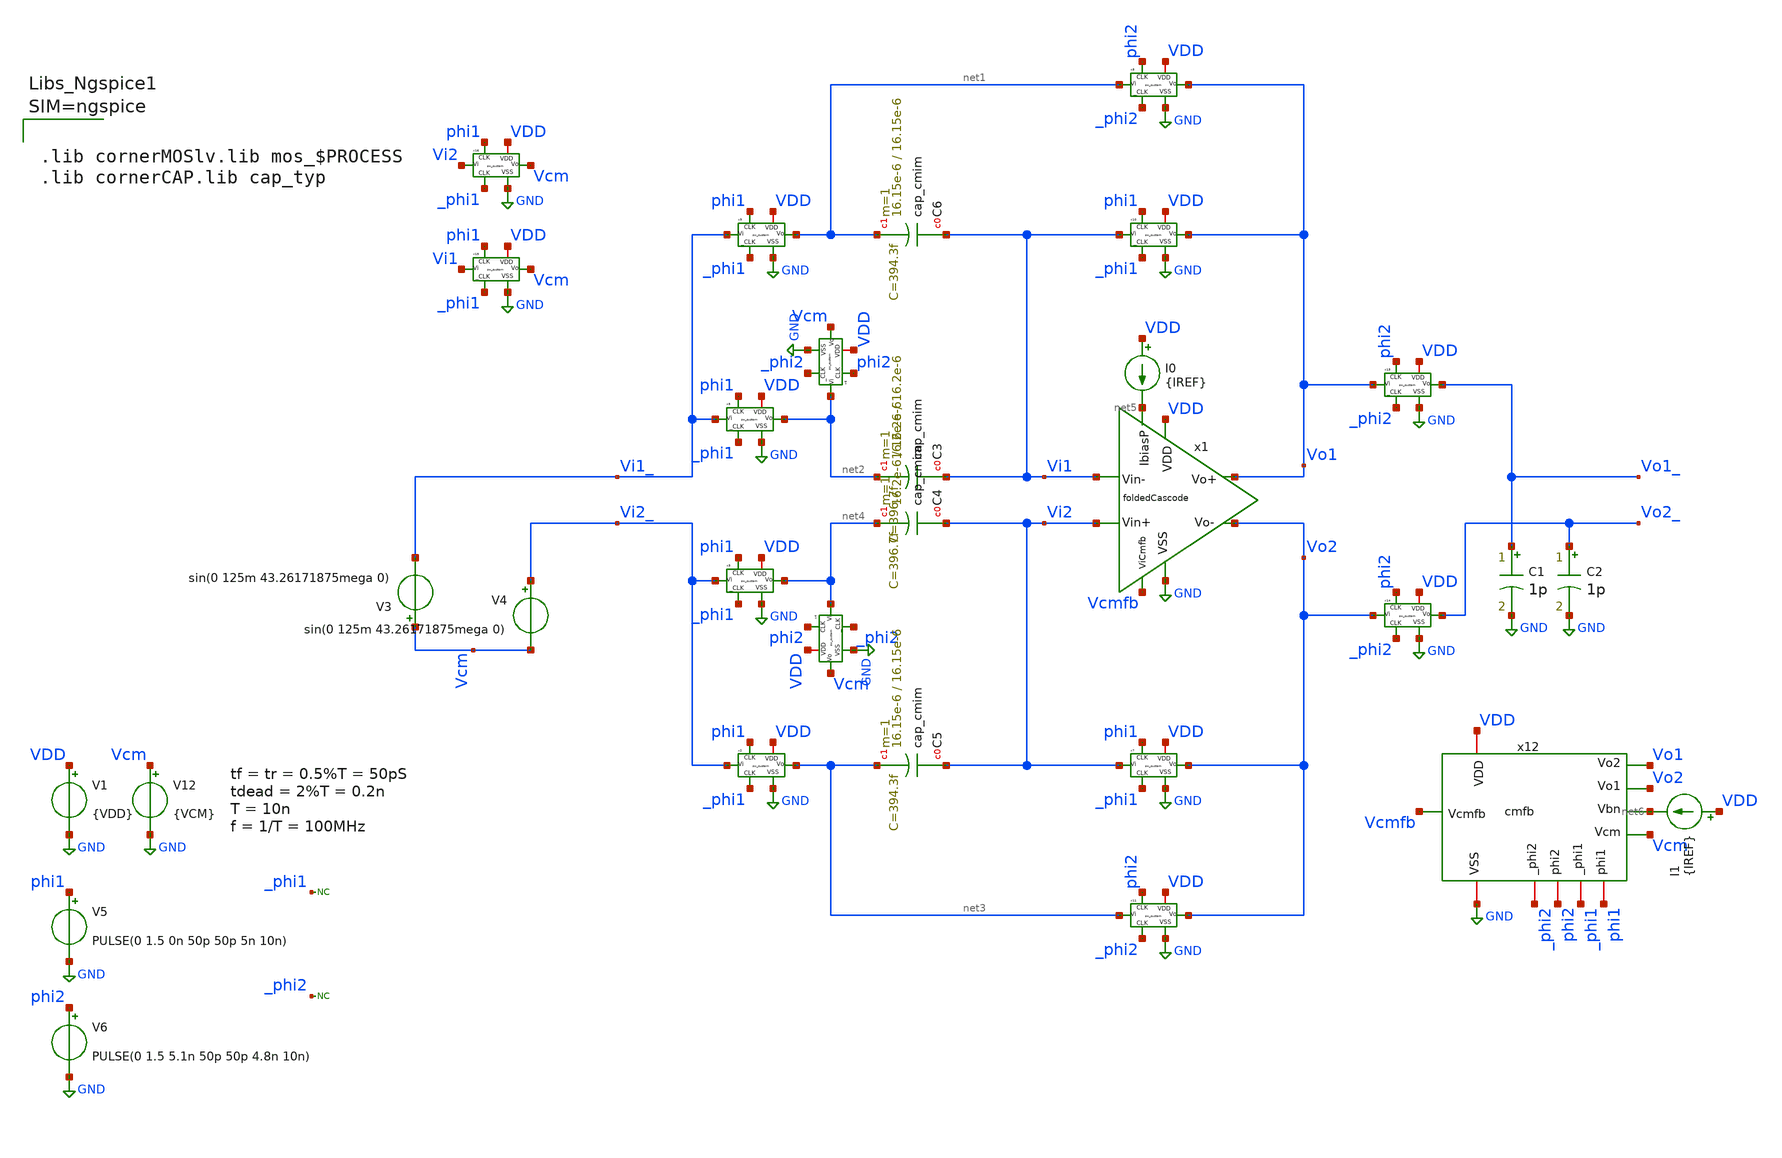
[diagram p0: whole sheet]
** sch_path: sch/AutoTestbench/tb/HFcloseLoop.sch
**.subckt HFcloseLoop
x1 VDD GND Vcmfb net5 Vo1 Vo2 Vi1 Vi2 foldedCascode
V1 VDD GND {VDD}
I0 VDD net5 {IREF}
V5 phi1 GND PULSE(0 1.5 0n 50p 50p 5n 10n)
V6 phi2 GND PULSE(0 1.5 5.1n 50p 50p 4.8n 10n)
x2 phi1 GND net3 Vi2_ VDD _phi1 sw_custom
x3 phi1 GND net4 Vi2_ VDD _phi1 sw_custom
x6 phi2 GND Vcm net2 VDD _phi2 sw_custom
x7 phi1 GND Vo2 Vi2 VDD _phi1 sw_custom
x8 phi2 GND Vo1 net1 VDD _phi2 sw_custom
x10 phi1 GND Vo1 Vi1 VDD _phi1 sw_custom
x9 phi1 GND net1 Vi1_ VDD _phi1 sw_custom
x11 phi2 GND Vo2 net3 VDD _phi2 sw_custom
x12 VDD GND phi1 _phi1 phi2 _phi2 Vcm net6 Vcmfb Vo2 Vo1 cmfb
x5 phi1 GND net2 Vi1_ VDD _phi1 sw_custom
x13 phi2 GND Vo1_ Vo1 VDD _phi2 sw_custom
x14 phi2 GND Vo2_ Vo2 VDD _phi2 sw_custom
V12 Vcm GND {VCM}
x15 phi1 GND Vcm Vi1 VDD _phi1 sw_custom
x16 phi1 GND Vcm Vi2 VDD _phi1 sw_custom
V3 Vcm Vi1_ sin(0 125m 43.26171875mega 0)
V4 Vi2_ Vcm sin(0 125m 43.26171875mega 0)
C1 Vo1_ GND 1p m=1
C2 Vo2_ GND 1p m=1
x4 phi2 GND Vcm net4 VDD _phi2 sw_custom
* noconn _phi1
* noconn _phi2
I1 VDD net6 {IREF}
XC3 Vi1 net2 cap_cmim w=16.2e-6 l=16.2e-6 m=1 mm_ok=1
XC5 Vi2 net3 cap_cmim w=16.15e-6 l=16.15e-6 m=1 mm_ok=1
XC6 Vi1 net1 cap_cmim w=16.15e-6 l=16.15e-6 m=1 mm_ok=1
XC4 Vi2 net4 cap_cmim w=16.2e-6 l=16.2e-6 m=1 mm_ok=1
**** begin user architecture code



.lib cornerMOSlv.lib mos_$PROCESS
.lib cornerCAP.lib cap_typ





.temp $TEMP
.model SW1 SW(Ron=200 Roff=10G Vt=0.4 Vh=0.1)
.nodeset v(Vo1)=0.6 v(Vo2)=0.6 v(Vi1)=0.6 v(Vi2)=0.6
.param VDD=$VDD
.param IREF=$IREF
.param VCM=$VCM
.control
op
tran 100p 12u
let vcm = (v(Vo1) + v(Vo2)) / 2
meas tran vcm_avg AVG vcm FROM=1u TO=3u
let Vinn = v(Vi1_)-v(Vi2_)
let Voutt = v(Vo1_)-v(Vo2_)
meas tran vin_pp  PP Vinn from=1u to=3u
meas tran vout_pp PP Voutt from=1u to=3u

let gain = vout_pp/vin_pp
print gain

let vcm_ = vcm_avg

echo Gain $&gain > results.txt
echo Vcm $&vcm_ >> results.txt

plot v(Vo1_)-v(Vo2_) v(phi2)

plot gain

write closeLoop.raw
*plot v(Vo1_) v(phi1)
plot v(Vo1_) v(Vi1_)
plot V(Vcmfb)
*plot v(Vo1)
plot v(vo1)
plot v(Vo1_)-v(Vo2_)
plot v(Vo1_) v(phi1) v(phi2)
*plot phi1 phi2


wrdata output.txt v(phi1) v(phi2) v(Vi1_) v(Vi2_) v(Vo1_) v(Vo2_) v(Vo1) v(Vi2)

.endc


**** end user architecture code
**.ends

* expanding   symbol:  foldedCascode.sym # of pins=8
** sym_path: sch/blocks/foldedCascode.sym
** sch_path: sch/blocks/foldedCascode.sch
.subckt foldedCascode VDD VSS ViCmfb IbiasP Vo+ Vo- Vin- Vin+
*.iopin VSS
*.iopin VDD
*.ipin ViCmfb
*.iopin IbiasP
*.ipin Vin+
*.ipin Vin-
*.iopin Vo+
*.iopin Vo-
x1 VDD Vb1_1 Vb1_2 Vx Vy VSS gmBoosting
XM0 net3 Vb0 VDD VDD sg13_lv_pmos w=70u l=0.3u ng=120 m=8 mm_ok=1
XM1 Vy Vin+ net3 net3 sg13_lv_pmos w=85u l=0.13u ng=100 m=2 mm_ok=1
XM2 Vx Vin- net3 net3 sg13_lv_pmos w=85u l=0.13u ng=100 m=2 mm_ok=1
XM7 Vo+ Vb2 net1 VDD sg13_lv_pmos w=47u l=0.4u ng=94 m=4 mm_ok=1
XM3 Vo+ Vb1_1 Vx VSS sg13_lv_nmos w=44u l=0.3u ng=22 m=6 mm_ok=1
XM8 Vo- Vb2 net2 VDD sg13_lv_pmos w=47u l=0.4u ng=94 m=4 mm_ok=1
XM12 Vx ViCmfb VSS VSS sg13_lv_nmos w=24.3u l=0.8u ng=62 m=6 mm_ok=1
XM4 Vo- Vb1_2 Vy VSS sg13_lv_nmos w=44u l=0.3u ng=22 m=6 mm_ok=1
XM5 Vy ViCmfb VSS VSS sg13_lv_nmos w=24.3u l=0.8u ng=62 m=6 mm_ok=1
I0 Vb0 VSS 10u
XM6 Vb0 Vb0 net4 VDD sg13_lv_pmos w=60u l=0.13u ng=10 m=1 mm_ok=1
XM13 net4 Vb0 VDD VDD sg13_lv_pmos w=11.5u l=0.3u ng=5 m=1 mm_ok=1
I1 Vb2 VSS 25u
XM18 Vb2 Vb2 net5 VDD sg13_lv_pmos w=18.5u l=0.7u ng=9 m=1 mm_ok=1
XM19 net5 Vb2 VDD VDD sg13_lv_pmos w=4u l=0.7u ng=1 m=1 mm_ok=1
XM20 Vb3 Vb2 net6 VDD sg13_lv_pmos w=5.5u l=0.4u ng=1 m=1 mm_ok=1
XM21 net6 Vb3 VDD VDD sg13_lv_pmos w=8.1u l=0.8u ng=1 m=1 mm_ok=1
I2 Vb3 VSS 10u
XM11 IbiasP IbiasP VSS VSS sg13_lv_nmos w=44u l=0.3u ng=22 m=6 mm_ok=1
XM9 net1 Vb3 VDD VDD sg13_lv_pmos w=62.2u l=0.8u ng=118 m=4 mm_ok=1
XM10 net2 Vb3 VDD VDD sg13_lv_pmos w=62.2u l=0.8u ng=118 m=4 mm_ok=1
.ends


* expanding   symbol:  sw_custom.sym # of pins=6
** sym_path: sch/blocks/sw_custom.sym
** sch_path: sch/blocks/sw_custom.sch
.subckt sw_custom CLK VSS Vo Vi VDD _CLK
*.iopin VSS
*.ipin CLK
*.ipin _CLK
*.iopin Vi
*.iopin Vo
*.iopin VDD
S1 Vi Vo CLK VSS SW1
.ends


* expanding   symbol:  cmfb.sym # of pins=11
** sym_path: sch/blocks/cmfb.sym
** sch_path: sch/blocks/cmfb.sch
.subckt cmfb VDD VSS phi1 _phi1 phi2 _phi2 Vcm Vbn Vcmfb Vo1 Vo2
*.iopin VDD
*.iopin VSS
*.iopin phi1
*.iopin _phi1
*.iopin phi2
*.iopin _phi2
*.ipin Vcm
*.ipin Vbn
*.opin Vcmfb
*.ipin Vo1
*.ipin Vo2
x15 phi1 VSS Vcmfb Vbn VDD _phi1 sw_custom
C6 net1 Vcmfb 100f m=1
x16 phi1 VSS net1 Vcm VDD _phi1 sw_custom
C7 net2 Vcmfb 100f m=1
x1 phi1 VSS net2 Vcm VDD _phi1 sw_custom
x2 phi2 VSS net2 Vo1 VDD _phi2 sw_custom
x3 phi2 VSS net1 Vo2 VDD _phi2 sw_custom
.ends


* expanding   symbol:  gmBoosting.sym # of pins=6
** sym_path: sch/blocks/gmBoosting.sym
** sch_path: sch/blocks/gmBoosting.sch
.subckt gmBoosting VDD Vo2 Vo1 Vi+ Vi- VSS
*.iopin VSS
*.opin Vo1
*.opin Vo2
*.ipin Vi+
*.ipin Vi-
*.iopin VDD
V1 Vref VSS 0.55
XM7 net2 Vb4 VDD VDD sg13_lv_pmos w=25u l=0.7u ng=13 m=2 mm_ok=1
XM1 net8 Vi+ net1 net1 sg13_lv_pmos w=40u l=0.15u ng=80 m=4 mm_ok=1
XM2 net4 Vi- net1 net1 sg13_lv_pmos w=40u l=0.15u ng=80 m=4 mm_ok=1
XM0 net1 Vb0 net5 VDD sg13_lv_pmos w=16u l=0.3u ng=20 m=1 mm_ok=1
XM6 net8 Vb3 VSS VSS sg13_lv_nmos w=20u l=0.7u ng=5 m=2 mm_ok=1
XM9 Vo1 Vb2 net2 VDD sg13_lv_pmos w=30u l=0.3u ng=10 m=1 mm_ok=1
XM10 Vo2 Vb2 net3 VDD sg13_lv_pmos w=30u l=0.3u ng=10 m=1 mm_ok=1
XM8 net3 Vb4 VDD VDD sg13_lv_pmos w=25u l=0.7u ng=13 m=2 mm_ok=1
XM3 net5 Vo2 VDD VDD sg13_lv_pmos w=20u l=0.13u ng=5 m=1 mm_ok=1
XM4 net5 Vo1 VDD VDD sg13_lv_pmos w=20u l=0.13u ng=5 m=1 mm_ok=1
XM5 net6 Vref VDD VDD sg13_lv_pmos w=20u l=0.13u ng=5 m=2 mm_ok=1
XM28 Vb0 net7 VSS VSS sg13_lv_nmos w=10u l=0.2u ng=2 m=1 mm_ok=1
XM29 Vb3 Vb3 VSS VSS sg13_lv_nmos w=30u l=0.2u ng=4 m=1 mm_ok=1
XR16 net7 Vb0 sub! rppd w=0.8e-6 l=2.5e-6 m=1 b=0 mm_ok=1
XM30 Vb3 Vb0 net6 VDD sg13_lv_pmos w=16u l=0.3u ng=20 m=1 mm_ok=1
XM31 net4 Vb3 VSS VSS sg13_lv_nmos w=20u l=0.7u ng=5 m=2 mm_ok=1
XM32 Vo1 Vb1 net4 VSS sg13_lv_nmos w=37.5u l=0.7u ng=5 m=1 mm_ok=1
XM33 Vo2 Vb1 net8 VSS sg13_lv_nmos w=37.5u l=0.7u ng=5 m=1 mm_ok=1
XM23 net7 Vbb VDD VDD sg13_lv_pmos w=18u l=1u ng=18 m=1 mm_ok=1
XR9 Vb1 net10 sub! rhigh w=0.5e-6 l=2.31e-6 m=1 b=0 mm_ok=1
XM17 net10 Vb1 net9 VSS sg13_lv_nmos w=25u l=0.7u ng=3 m=1 mm_ok=1
XM18 net9 net10 VSS VSS sg13_lv_nmos w=40u l=0.7u ng=4 m=1 mm_ok=1
XM19 net11 Vb4 VDD VDD sg13_lv_pmos w=15u l=0.7u ng=5 m=1 mm_ok=1
XM20 Vb4 Vb2 net11 VDD sg13_lv_pmos w=7u l=0.3u ng=7 m=1 mm_ok=1
XR10 Vb4 Vb2 sub! rhigh w=0.5e-6 l=1.8e-6 m=1 b=0 mm_ok=1
I3 Vbb VSS 50u
XM21 Vbb Vbb VDD VDD sg13_lv_pmos w=18u l=1u ng=18 m=1 mm_ok=1
XM22 Vb1 Vbb VDD VDD sg13_lv_pmos w=18u l=1u ng=18 m=1 mm_ok=1
XM24 net12 Vbb VDD VDD sg13_lv_pmos w=18u l=1u ng=18 m=1 mm_ok=1
XM25 net12 net12 VSS VSS sg13_lv_nmos w=15u l=1u ng=2 m=1 mm_ok=1
XM26 Vb2 net12 VSS VSS sg13_lv_nmos w=15u l=1u ng=2 m=1 mm_ok=1
.ends

.GLOBAL GND
**** begin user architecture code
.MODEL SW1 SW   VT=0.9 VH=0.01  RON=0.01 ROFF=10G
**** end user architecture code
.end
